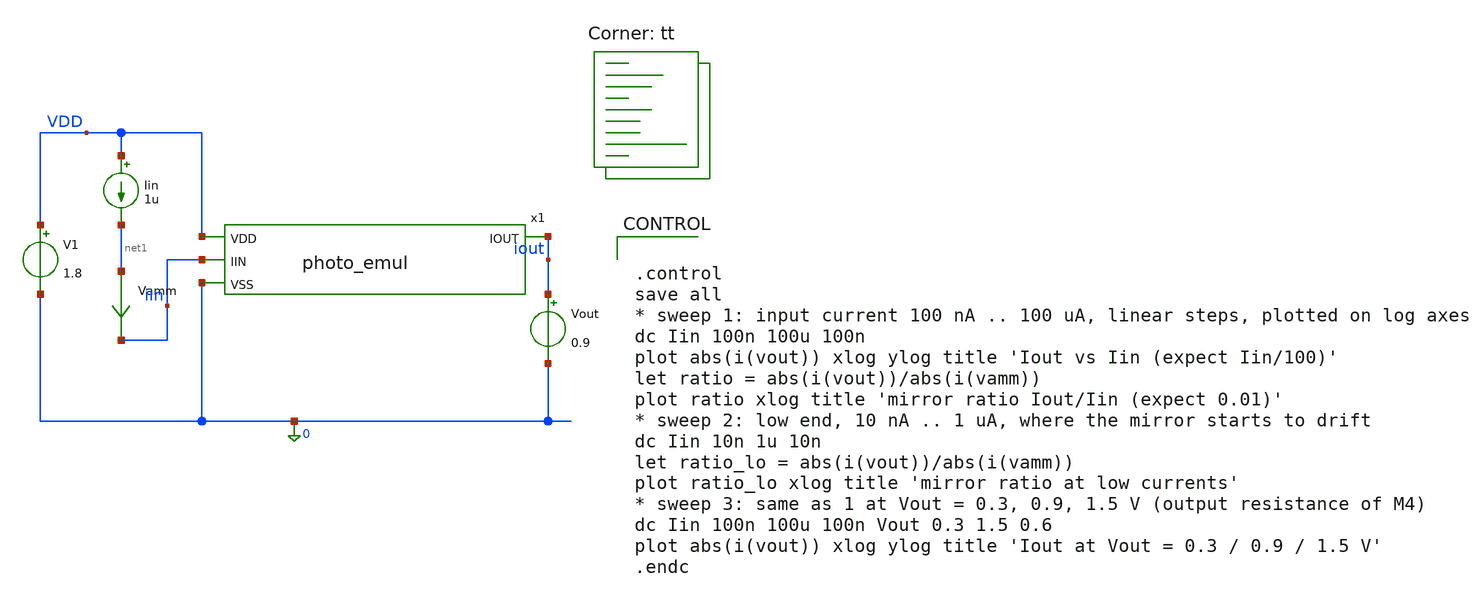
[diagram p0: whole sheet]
** sch_path: xschem/testbench_emul.sch
**.subckt testbench_emul
x1 VDD iin iout 0 photo_emul
Vamm net1 iin 0
.save i(vamm)
V1 VDD 0 1.8
Iin VDD net1 1u
Vout iout 0 0.9
**** begin user architecture code
.lib $::SKYWATER_MODELS/sky130.lib.spice tt


.control
save all
* sweep 1: input current 100 nA .. 100 uA, linear steps, plotted on log axes
dc Iin 100n 100u 100n
plot abs(i(vout)) xlog ylog title 'Iout vs Iin (expect Iin/100)'
let ratio = abs(i(vout))/abs(i(vamm))
plot ratio xlog title 'mirror ratio Iout/Iin (expect 0.01)'
* sweep 2: low end, 10 nA .. 1 uA, where the mirror starts to drift
dc Iin 10n 1u 10n
let ratio_lo = abs(i(vout))/abs(i(vamm))
plot ratio_lo xlog title 'mirror ratio at low currents'
* sweep 3: same as 1 at Vout = 0.3, 0.9, 1.5 V (output resistance of M4)
dc Iin 100n 100u 100n Vout 0.3 1.5 0.6
plot abs(i(vout)) xlog ylog title 'Iout at Vout = 0.3 / 0.9 / 1.5 V'
.endc


**** end user architecture code
**.ends
.end
